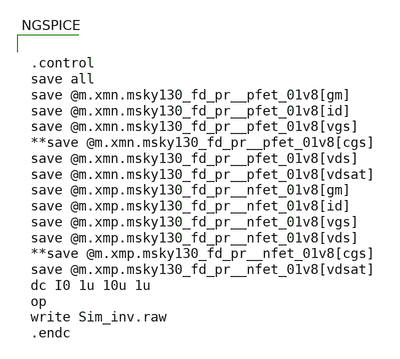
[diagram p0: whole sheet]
** sch_path: ISSCC25/submitted_notebooks/current_mirror_ota_optimization/characterization/sky130/xschem_cds/schematics/test_symbols.sch
**.subckt test_symbols
**** begin user architecture code


.control
save all
save @m.xmn.msky130_fd_pr__pfet_01v8[gm]
save @m.xmn.msky130_fd_pr__pfet_01v8[id]
save @m.xmn.msky130_fd_pr__pfet_01v8[vgs]
**save @m.xmn.msky130_fd_pr__pfet_01v8[cgs]
save @m.xmn.msky130_fd_pr__pfet_01v8[vds]
save @m.xmn.msky130_fd_pr__pfet_01v8[vdsat]
save @m.xmp.msky130_fd_pr__nfet_01v8[gm]
save @m.xmp.msky130_fd_pr__nfet_01v8[id]
save @m.xmp.msky130_fd_pr__nfet_01v8[vgs]
save @m.xmp.msky130_fd_pr__nfet_01v8[vds]
**save @m.xmp.msky130_fd_pr__nfet_01v8[cgs]
save @m.xmp.msky130_fd_pr__nfet_01v8[vdsat]
dc I0 1u 10u 1u
op
write Sim_inv.raw
.endc


**** end user architecture code
**.ends
.end
